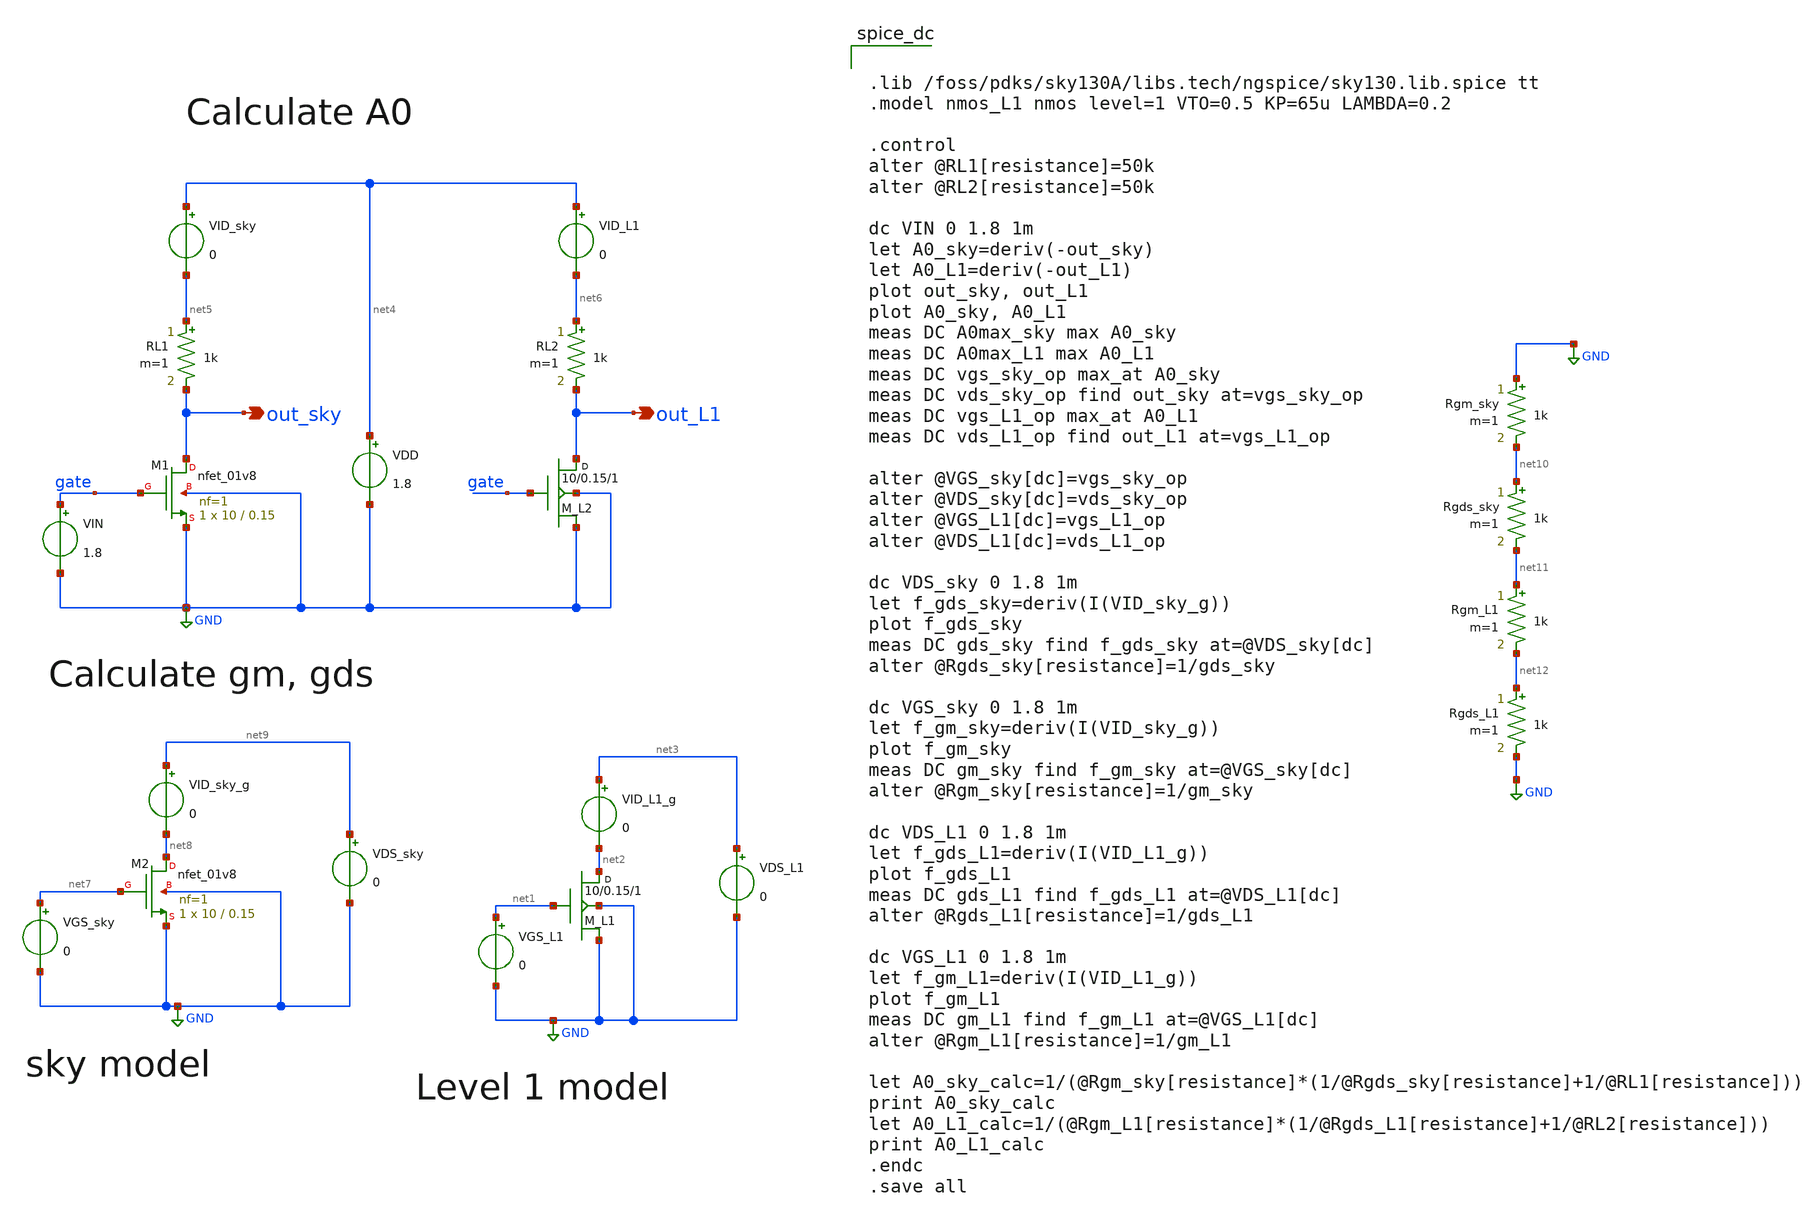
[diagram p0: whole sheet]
** sch_path: designs/reference/nmost_calc_gdsgm_TEUE.sch
**.subckt nmost_calc_gdsgm_TEUE out_sky out_L1
*.opin out_sky
*.opin out_L1
M_L1 net2 net1 GND GND nmos_L1 w=10 l=0.15 m=1
VID_L1_g net3 net2 0
VDS_L1 net3 GND 0
VGS_L1 net1 GND 0
XM1 out_sky gate GND GND sky130_fd_pr__nfet_01v8 L=0.15 W=10 nf=1 ad='int((nf+1)/2) * W/nf * 0.29' as='int((nf+2)/2) * W/nf * 0.29'
+ pd='2*int((nf+1)/2) * (W/nf + 0.29)' ps='2*int((nf+2)/2) * (W/nf + 0.29)' nrd='0.29 / W' nrs='0.29 / W'
+ sa=0 sb=0 sd=0 mult=1 m=1
VIN gate GND 1.8
VDD net4 GND 1.8
VID_sky net4 net5 0
M_L2 out_L1 gate GND GND nmos_L1 w=10 l=0.15 m=1
VID_L1 net4 net6 0
RL1 net5 out_sky 1k m=1
RL2 net6 out_L1 1k m=1
XM2 net8 net7 GND GND sky130_fd_pr__nfet_01v8 L=0.15 W=10 nf=1 ad='int((nf+1)/2) * W/nf * 0.29' as='int((nf+2)/2) * W/nf * 0.29'
+ pd='2*int((nf+1)/2) * (W/nf + 0.29)' ps='2*int((nf+2)/2) * (W/nf + 0.29)' nrd='0.29 / W' nrs='0.29 / W'
+ sa=0 sb=0 sd=0 mult=1 m=1
VGS_sky net7 GND 0
VDS_sky net9 GND 0
VID_sky_g net9 net8 0
Rgds_L1 net12 GND 1k m=1
Rgm_L1 net11 net12 1k m=1
Rgds_sky net10 net11 1k m=1
Rgm_sky GND net10 1k m=1
**** begin user architecture code


.lib /foss/pdks/sky130A/libs.tech/ngspice/sky130.lib.spice tt
.model nmos_L1 nmos level=1 VTO=0.5 KP=65u LAMBDA=0.2

.control
alter @RL1[resistance]=50k
alter @RL2[resistance]=50k

dc VIN 0 1.8 1m
let A0_sky=deriv(-out_sky)
let A0_L1=deriv(-out_L1)
plot out_sky, out_L1
plot A0_sky, A0_L1
meas DC A0max_sky max A0_sky
meas DC A0max_L1 max A0_L1
meas DC vgs_sky_op max_at A0_sky
meas DC vds_sky_op find out_sky at=vgs_sky_op
meas DC vgs_L1_op max_at A0_L1
meas DC vds_L1_op find out_L1 at=vgs_L1_op

alter @VGS_sky[dc]=vgs_sky_op
alter @VDS_sky[dc]=vds_sky_op
alter @VGS_L1[dc]=vgs_L1_op
alter @VDS_L1[dc]=vds_L1_op

dc VDS_sky 0 1.8 1m
let f_gds_sky=deriv(I(VID_sky_g))
plot f_gds_sky
meas DC gds_sky find f_gds_sky at=@VDS_sky[dc]
alter @Rgds_sky[resistance]=1/gds_sky

dc VGS_sky 0 1.8 1m
let f_gm_sky=deriv(I(VID_sky_g))
plot f_gm_sky
meas DC gm_sky find f_gm_sky at=@VGS_sky[dc]
alter @Rgm_sky[resistance]=1/gm_sky

dc VDS_L1 0 1.8 1m
let f_gds_L1=deriv(I(VID_L1_g))
plot f_gds_L1
meas DC gds_L1 find f_gds_L1 at=@VDS_L1[dc]
alter @Rgds_L1[resistance]=1/gds_L1

dc VGS_L1 0 1.8 1m
let f_gm_L1=deriv(I(VID_L1_g))
plot f_gm_L1
meas DC gm_L1 find f_gm_L1 at=@VGS_L1[dc]
alter @Rgm_L1[resistance]=1/gm_L1

let A0_sky_calc=1/(@Rgm_sky[resistance]*(1/@Rgds_sky[resistance]+1/@RL1[resistance]))
print A0_sky_calc
let A0_L1_calc=1/(@Rgm_L1[resistance]*(1/@Rgds_L1[resistance]+1/@RL2[resistance]))
print A0_L1_calc
.endc
.save all

**** end user architecture code
**.ends
.GLOBAL GND
.end
